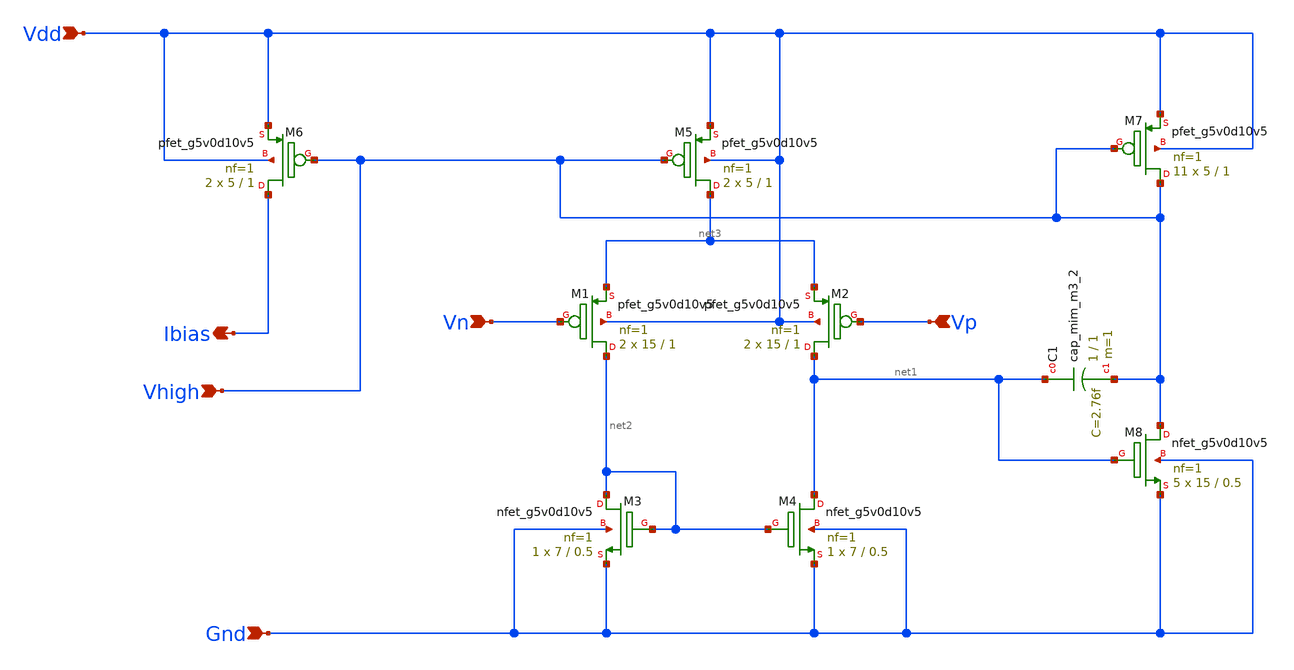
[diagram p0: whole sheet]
** sch_path: Analog_blocks/Analog_Blocks/Bandgap/Schematics/BGR5v/Bandgap5v_OTA.sch
**.subckt Bandgap5v_OTA Ibias Vhigh Vdd Gnd Vp Vn
*.opin Ibias
*.ipin Vhigh
*.ipin Vdd
*.ipin Gnd
*.ipin Vp
*.ipin Vn
XM6 Ibias Vhigh Vdd Vdd sky130_fd_pr__pfet_g5v0d10v5 L=1 W=5 nf=1 ad='int((nf+1)/2) * W/nf * 0.29' as='int((nf+2)/2) * W/nf * 0.29'
+ pd='2*int((nf+1)/2) * (W/nf + 0.29)' ps='2*int((nf+2)/2) * (W/nf + 0.29)' nrd='0.29 / W' nrs='0.29 / W'
+ sa=0 sb=0 sd=0 mult=2 m=2
XM5 net3 Vhigh Vdd Vdd sky130_fd_pr__pfet_g5v0d10v5 L=1 W=5 nf=1 ad='int((nf+1)/2) * W/nf * 0.29' as='int((nf+2)/2) * W/nf * 0.29'
+ pd='2*int((nf+1)/2) * (W/nf + 0.29)' ps='2*int((nf+2)/2) * (W/nf + 0.29)' nrd='0.29 / W' nrs='0.29 / W'
+ sa=0 sb=0 sd=0 mult=2 m=2
XM7 Vhigh Vhigh Vdd Vdd sky130_fd_pr__pfet_g5v0d10v5 L=1 W=5 nf=1 ad='int((nf+1)/2) * W/nf * 0.29' as='int((nf+2)/2) * W/nf * 0.29'
+ pd='2*int((nf+1)/2) * (W/nf + 0.29)' ps='2*int((nf+2)/2) * (W/nf + 0.29)' nrd='0.29 / W' nrs='0.29 / W'
+ sa=0 sb=0 sd=0 mult=11 m=11
XM2 net1 Vp net3 Vdd sky130_fd_pr__pfet_g5v0d10v5 L=1 W=15 nf=1 ad='int((nf+1)/2) * W/nf * 0.29' as='int((nf+2)/2) * W/nf * 0.29'
+ pd='2*int((nf+1)/2) * (W/nf + 0.29)' ps='2*int((nf+2)/2) * (W/nf + 0.29)' nrd='0.29 / W' nrs='0.29 / W'
+ sa=0 sb=0 sd=0 mult=2 m=2
XM1 net2 Vn net3 Vdd sky130_fd_pr__pfet_g5v0d10v5 L=1 W=15 nf=1 ad='int((nf+1)/2) * W/nf * 0.29' as='int((nf+2)/2) * W/nf * 0.29'
+ pd='2*int((nf+1)/2) * (W/nf + 0.29)' ps='2*int((nf+2)/2) * (W/nf + 0.29)' nrd='0.29 / W' nrs='0.29 / W'
+ sa=0 sb=0 sd=0 mult=2 m=2
XM8 Vhigh net1 Gnd Gnd sky130_fd_pr__nfet_g5v0d10v5 L=0.5 W=15 nf=1 ad='int((nf+1)/2) * W/nf * 0.29'
+ as='int((nf+2)/2) * W/nf * 0.29' pd='2*int((nf+1)/2) * (W/nf + 0.29)' ps='2*int((nf+2)/2) * (W/nf + 0.29)'
+ nrd='0.29 / W' nrs='0.29 / W' sa=0 sb=0 sd=0 mult=5 m=5
XM4 net1 net2 Gnd Gnd sky130_fd_pr__nfet_g5v0d10v5 L=0.5 W=7 nf=1 ad='int((nf+1)/2) * W/nf * 0.29' as='int((nf+2)/2) * W/nf * 0.29'
+ pd='2*int((nf+1)/2) * (W/nf + 0.29)' ps='2*int((nf+2)/2) * (W/nf + 0.29)' nrd='0.29 / W' nrs='0.29 / W'
+ sa=0 sb=0 sd=0 mult=1 m=1
XM3 net2 net2 Gnd Gnd sky130_fd_pr__nfet_g5v0d10v5 L=0.5 W=7 nf=1 ad='int((nf+1)/2) * W/nf * 0.29' as='int((nf+2)/2) * W/nf * 0.29'
+ pd='2*int((nf+1)/2) * (W/nf + 0.29)' ps='2*int((nf+2)/2) * (W/nf + 0.29)' nrd='0.29 / W' nrs='0.29 / W'
+ sa=0 sb=0 sd=0 mult=1 m=1
XC1 net1 Vhigh sky130_fd_pr__cap_mim_m3_2 W=1 L=1 MF=1 m=1
**.ends
.end
